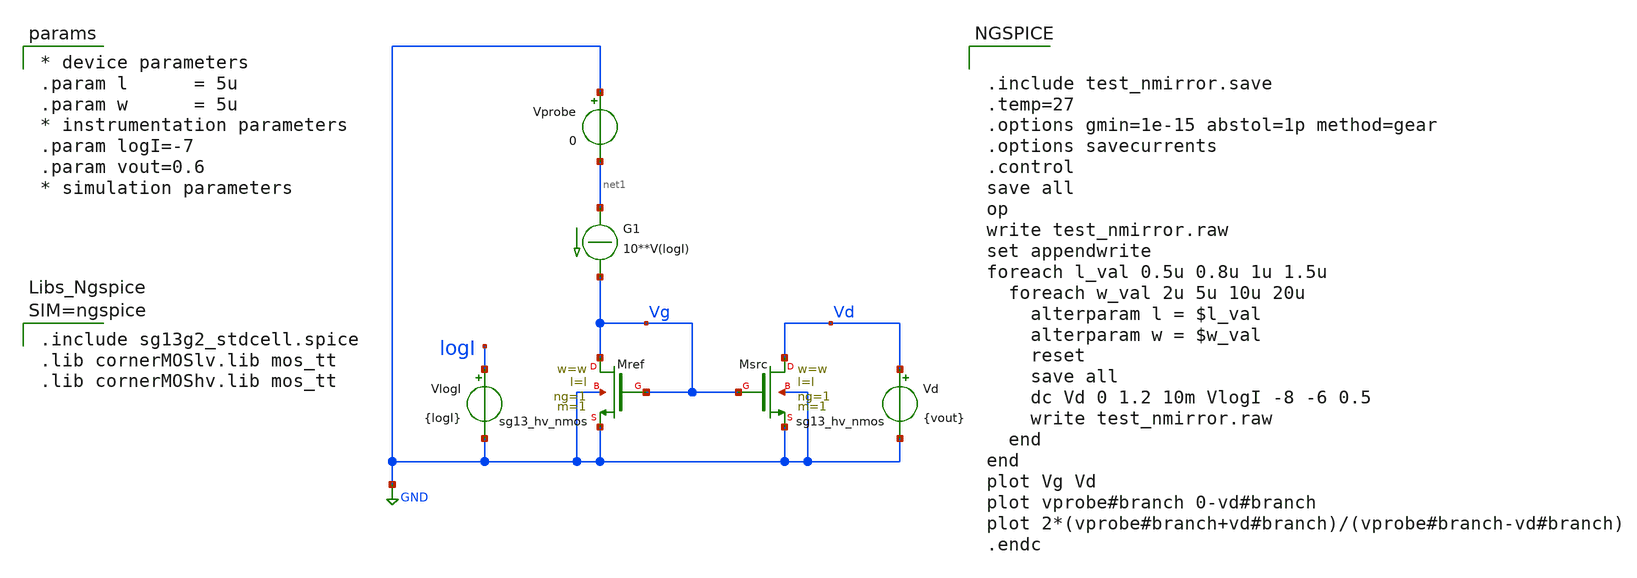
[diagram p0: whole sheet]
** sch_path: xschem/test_nmirror.sch
**.subckt test_nmirror
XMsrc Vd Vg GND GND sg13_hv_nmos w=w l=l ng=1 m=1 mm_ok=1
XMref Vg Vg GND GND sg13_hv_nmos w=w l=l ng=1 m=1 mm_ok=1
Vprobe GND net1 0
.save i(vprobe)
G1 net1 Vg CUR=' 10**V(logI) '
VlogI logI GND {logI}
.save i(vlogi)
Vd Vd GND {vout}
.save i(vd)
**** begin user architecture code


.include sg13g2_stdcell.spice
.lib cornerMOSlv.lib mos_tt
.lib cornerMOShv.lib mos_tt



* device parameters
.param l      = 5u
.param w      = 5u
* instrumentation parameters
.param logI=-7
.param vout=0.6
* simulation parameters




.include test_nmirror.save
.temp=27
.options gmin=1e-15 abstol=1p method=gear
.options savecurrents
.control
save all
op
write test_nmirror.raw
set appendwrite
foreach l_val 0.5u 0.8u 1u 1.5u
  foreach w_val 2u 5u 10u 20u
    alterparam l = $l_val
    alterparam w = $w_val
    reset
    save all
    dc Vd 0 1.2 10m VlogI -8 -6 0.5
    write test_nmirror.raw
  end
end
plot Vg Vd
plot vprobe#branch 0-vd#branch
plot 2*(vprobe#branch+vd#branch)/(vprobe#branch-vd#branch)
.endc


**** end user architecture code
**.ends
.GLOBAL GND
.end
